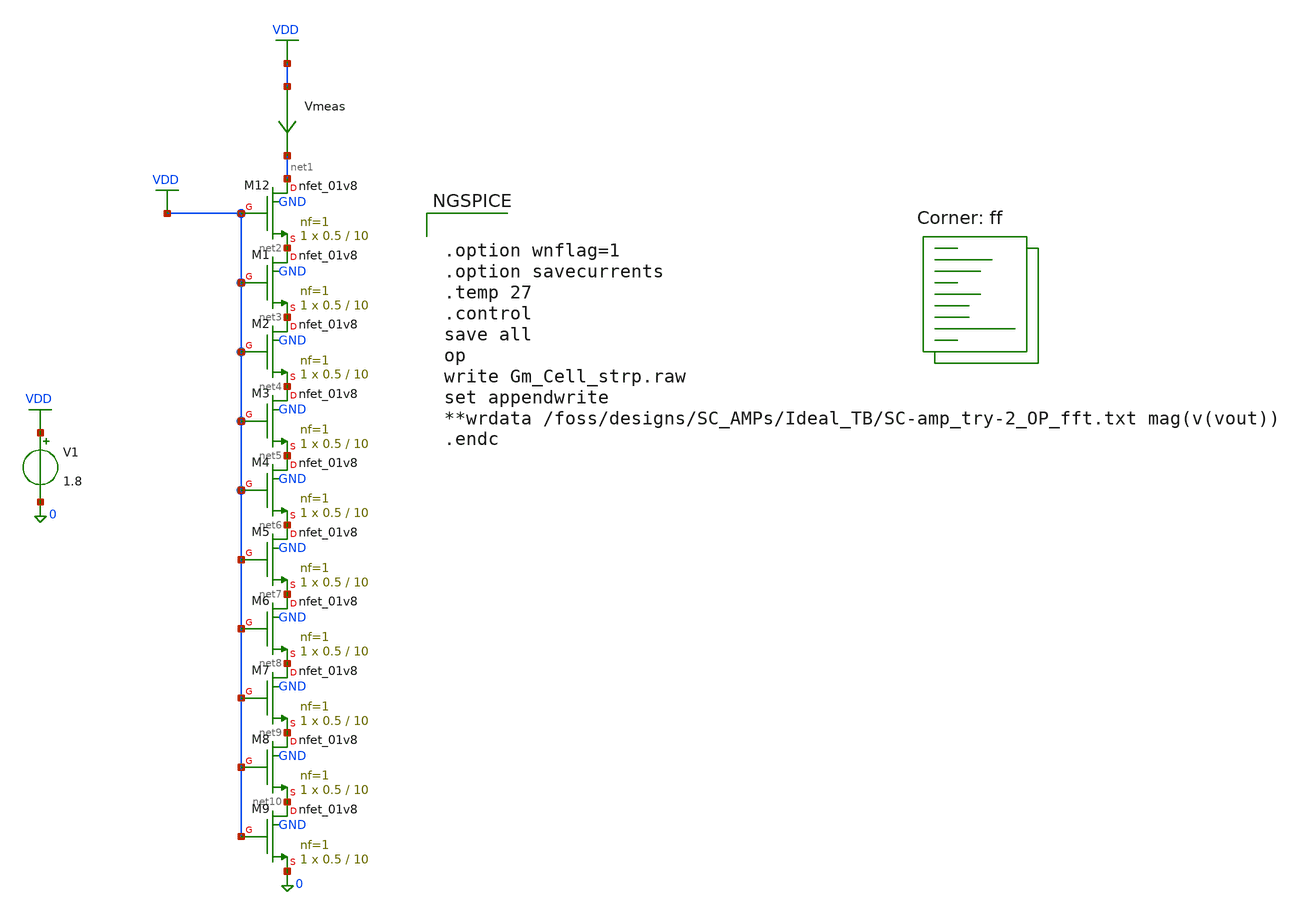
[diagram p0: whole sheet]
** sch_path: OTAs/NMOS_SrcDeg_SE_OTA_IntBias/SCH/Gm_Cell_strp.sch
**.subckt Gm_Cell_strp
XM12 net1 VDD net2 GND sky130_fd_pr__nfet_01v8 L=10 W=0.5 nf=1 ad='int((1 + 1)/2) * 0.5 / 1 * 0.29' as='int((1 + 2)/2) * 0.5 / 1 * 0.29'
+ pd='2*int((1 + 1)/2) * (0.5 / 1 + 0.29)' ps='2*int((1 + 2)/2) * (0.5 / 1 + 0.29)' nrd='0.29 / 0.5 ' nrs='0.29 / 0.5 '
+ sa=0 sb=0 sd=0 mult=1 m=1
V1 VDD 0 1.8
Vmeas VDD net1 0
.save i(vmeas)
XM1 net2 VDD net3 GND sky130_fd_pr__nfet_01v8 L=10 W=0.5 nf=1 ad='int((1 + 1)/2) * 0.5 / 1 * 0.29' as='int((1 + 2)/2) * 0.5 / 1 * 0.29'
+ pd='2*int((1 + 1)/2) * (0.5 / 1 + 0.29)' ps='2*int((1 + 2)/2) * (0.5 / 1 + 0.29)' nrd='0.29 / 0.5 ' nrs='0.29 / 0.5 '
+ sa=0 sb=0 sd=0 mult=1 m=1
XM2 net3 VDD net4 GND sky130_fd_pr__nfet_01v8 L=10 W=0.5 nf=1 ad='int((1 + 1)/2) * 0.5 / 1 * 0.29' as='int((1 + 2)/2) * 0.5 / 1 * 0.29'
+ pd='2*int((1 + 1)/2) * (0.5 / 1 + 0.29)' ps='2*int((1 + 2)/2) * (0.5 / 1 + 0.29)' nrd='0.29 / 0.5 ' nrs='0.29 / 0.5 '
+ sa=0 sb=0 sd=0 mult=1 m=1
XM3 net4 VDD net5 GND sky130_fd_pr__nfet_01v8 L=10 W=0.5 nf=1 ad='int((1 + 1)/2) * 0.5 / 1 * 0.29' as='int((1 + 2)/2) * 0.5 / 1 * 0.29'
+ pd='2*int((1 + 1)/2) * (0.5 / 1 + 0.29)' ps='2*int((1 + 2)/2) * (0.5 / 1 + 0.29)' nrd='0.29 / 0.5 ' nrs='0.29 / 0.5 '
+ sa=0 sb=0 sd=0 mult=1 m=1
XM4 net5 VDD net6 GND sky130_fd_pr__nfet_01v8 L=10 W=0.5 nf=1 ad='int((1 + 1)/2) * 0.5 / 1 * 0.29' as='int((1 + 2)/2) * 0.5 / 1 * 0.29'
+ pd='2*int((1 + 1)/2) * (0.5 / 1 + 0.29)' ps='2*int((1 + 2)/2) * (0.5 / 1 + 0.29)' nrd='0.29 / 0.5 ' nrs='0.29 / 0.5 '
+ sa=0 sb=0 sd=0 mult=1 m=1
XM5 net6 VDD net7 GND sky130_fd_pr__nfet_01v8 L=10 W=0.5 nf=1 ad='int((1 + 1)/2) * 0.5 / 1 * 0.29' as='int((1 + 2)/2) * 0.5 / 1 * 0.29'
+ pd='2*int((1 + 1)/2) * (0.5 / 1 + 0.29)' ps='2*int((1 + 2)/2) * (0.5 / 1 + 0.29)' nrd='0.29 / 0.5 ' nrs='0.29 / 0.5 '
+ sa=0 sb=0 sd=0 mult=1 m=1
XM6 net7 VDD net8 GND sky130_fd_pr__nfet_01v8 L=10 W=0.5 nf=1 ad='int((1 + 1)/2) * 0.5 / 1 * 0.29' as='int((1 + 2)/2) * 0.5 / 1 * 0.29'
+ pd='2*int((1 + 1)/2) * (0.5 / 1 + 0.29)' ps='2*int((1 + 2)/2) * (0.5 / 1 + 0.29)' nrd='0.29 / 0.5 ' nrs='0.29 / 0.5 '
+ sa=0 sb=0 sd=0 mult=1 m=1
XM7 net8 VDD net9 GND sky130_fd_pr__nfet_01v8 L=10 W=0.5 nf=1 ad='int((1 + 1)/2) * 0.5 / 1 * 0.29' as='int((1 + 2)/2) * 0.5 / 1 * 0.29'
+ pd='2*int((1 + 1)/2) * (0.5 / 1 + 0.29)' ps='2*int((1 + 2)/2) * (0.5 / 1 + 0.29)' nrd='0.29 / 0.5 ' nrs='0.29 / 0.5 '
+ sa=0 sb=0 sd=0 mult=1 m=1
XM8 net9 VDD net10 GND sky130_fd_pr__nfet_01v8 L=10 W=0.5 nf=1 ad='int((1 + 1)/2) * 0.5 / 1 * 0.29' as='int((1 + 2)/2) * 0.5 / 1 * 0.29'
+ pd='2*int((1 + 1)/2) * (0.5 / 1 + 0.29)' ps='2*int((1 + 2)/2) * (0.5 / 1 + 0.29)' nrd='0.29 / 0.5 ' nrs='0.29 / 0.5 '
+ sa=0 sb=0 sd=0 mult=1 m=1
XM9 net10 VDD 0 GND sky130_fd_pr__nfet_01v8 L=10 W=0.5 nf=1 ad='int((1 + 1)/2) * 0.5 / 1 * 0.29' as='int((1 + 2)/2) * 0.5 / 1 * 0.29'
+ pd='2*int((1 + 1)/2) * (0.5 / 1 + 0.29)' ps='2*int((1 + 2)/2) * (0.5 / 1 + 0.29)' nrd='0.29 / 0.5 ' nrs='0.29 / 0.5 '
+ sa=0 sb=0 sd=0 mult=1 m=1
**** begin user architecture code


.option wnflag=1
.option savecurrents
.temp 27
.control
save all
op
write Gm_Cell_strp.raw
set appendwrite
**wrdata /foss/designs/SC_AMPs/Ideal_TB/SC-amp_try-2_OP_fft.txt mag(v(vout))
.endc





.save @m.xm12.msky130_fd_pr__nfet_01v8[gm]
.save @m.xm12.msky130_fd_pr__nfet_01v8[gds]
.save @m.xm12.msky130_fd_pr__nfet_01v8[vth]
.save @m.xm12.msky130_fd_pr__nfet_01v8[vdsat]
.save @m.xm12.msky130_fd_pr__nfet_01v8[cgg]
.save @m.xm12.msky130_fd_pr__nfet_01v8[cgso]
.save @m.xm12.msky130_fd_pr__nfet_01v8[cgdo]
.save @m.xm1.msky130_fd_pr__nfet_01v8[gm]
.save @m.xm1.msky130_fd_pr__nfet_01v8[gds]
.save @m.xm1.msky130_fd_pr__nfet_01v8[vth]
.save @m.xm1.msky130_fd_pr__nfet_01v8[vdsat]
.save @m.xm1.msky130_fd_pr__nfet_01v8[cgg]
.save @m.xm1.msky130_fd_pr__nfet_01v8[cgso]
.save @m.xm1.msky130_fd_pr__nfet_01v8[cgdo]
.save @m.xm2.msky130_fd_pr__nfet_01v8[gm]
.save @m.xm2.msky130_fd_pr__nfet_01v8[gds]
.save @m.xm2.msky130_fd_pr__nfet_01v8[vth]
.save @m.xm2.msky130_fd_pr__nfet_01v8[vdsat]
.save @m.xm2.msky130_fd_pr__nfet_01v8[cgg]
.save @m.xm2.msky130_fd_pr__nfet_01v8[cgso]
.save @m.xm2.msky130_fd_pr__nfet_01v8[cgdo]
.save @m.xm3.msky130_fd_pr__nfet_01v8[gm]
.save @m.xm3.msky130_fd_pr__nfet_01v8[gds]
.save @m.xm3.msky130_fd_pr__nfet_01v8[vth]
.save @m.xm3.msky130_fd_pr__nfet_01v8[vdsat]
.save @m.xm3.msky130_fd_pr__nfet_01v8[cgg]
.save @m.xm3.msky130_fd_pr__nfet_01v8[cgso]
.save @m.xm3.msky130_fd_pr__nfet_01v8[cgdo]
.save @m.xm4.msky130_fd_pr__nfet_01v8[gm]
.save @m.xm4.msky130_fd_pr__nfet_01v8[gds]
.save @m.xm4.msky130_fd_pr__nfet_01v8[vth]
.save @m.xm4.msky130_fd_pr__nfet_01v8[vdsat]
.save @m.xm4.msky130_fd_pr__nfet_01v8[cgg]
.save @m.xm4.msky130_fd_pr__nfet_01v8[cgso]
.save @m.xm4.msky130_fd_pr__nfet_01v8[cgdo]
.save @m.xm5.msky130_fd_pr__nfet_01v8[gm]
.save @m.xm5.msky130_fd_pr__nfet_01v8[gds]
.save @m.xm5.msky130_fd_pr__nfet_01v8[vth]
.save @m.xm5.msky130_fd_pr__nfet_01v8[vdsat]
.save @m.xm5.msky130_fd_pr__nfet_01v8[cgg]
.save @m.xm5.msky130_fd_pr__nfet_01v8[cgso]
.save @m.xm5.msky130_fd_pr__nfet_01v8[cgdo]
.save @m.xm6.msky130_fd_pr__nfet_01v8[gm]
.save @m.xm6.msky130_fd_pr__nfet_01v8[gds]
.save @m.xm6.msky130_fd_pr__nfet_01v8[vth]
.save @m.xm6.msky130_fd_pr__nfet_01v8[vdsat]
.save @m.xm6.msky130_fd_pr__nfet_01v8[cgg]
.save @m.xm6.msky130_fd_pr__nfet_01v8[cgso]
.save @m.xm6.msky130_fd_pr__nfet_01v8[cgdo]
.save @m.xm7.msky130_fd_pr__nfet_01v8[gm]
.save @m.xm7.msky130_fd_pr__nfet_01v8[gds]
.save @m.xm7.msky130_fd_pr__nfet_01v8[vth]
.save @m.xm7.msky130_fd_pr__nfet_01v8[vdsat]
.save @m.xm7.msky130_fd_pr__nfet_01v8[cgg]
.save @m.xm7.msky130_fd_pr__nfet_01v8[cgso]
.save @m.xm7.msky130_fd_pr__nfet_01v8[cgdo]
.save @m.xm8.msky130_fd_pr__nfet_01v8[gm]
.save @m.xm8.msky130_fd_pr__nfet_01v8[gds]
.save @m.xm8.msky130_fd_pr__nfet_01v8[vth]
.save @m.xm8.msky130_fd_pr__nfet_01v8[vdsat]
.save @m.xm8.msky130_fd_pr__nfet_01v8[cgg]
.save @m.xm8.msky130_fd_pr__nfet_01v8[cgso]
.save @m.xm8.msky130_fd_pr__nfet_01v8[cgdo]
.save @m.xm9.msky130_fd_pr__nfet_01v8[gm]
.save @m.xm9.msky130_fd_pr__nfet_01v8[gds]
.save @m.xm9.msky130_fd_pr__nfet_01v8[vth]
.save @m.xm9.msky130_fd_pr__nfet_01v8[vdsat]
.save @m.xm9.msky130_fd_pr__nfet_01v8[cgg]
.save @m.xm9.msky130_fd_pr__nfet_01v8[cgso]
.save @m.xm9.msky130_fd_pr__nfet_01v8[cgdo]


.lib $::SKYWATER_MODELS/sky130.lib.spice ff
**** end user architecture code
**.ends
.GLOBAL VDD
.end
